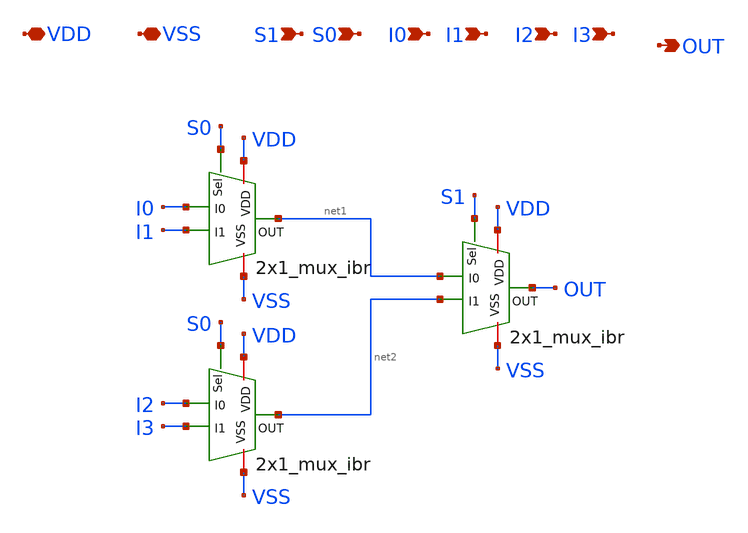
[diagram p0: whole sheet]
** sch_path: Clock_Generator_PAKISTAN_02/Schematics/4x1_mux_ibr..sch
**.subckt 4x1_mux_ibr. VDD VSS S1 OUT I2 I3 S0 I0 I1
*.iopin VDD
*.iopin VSS
*.ipin S1
*.opin OUT
*.ipin I2
*.ipin I3
*.ipin S0
*.ipin I0
*.ipin I1
x1 VSS S0 net1 I0 I1 VDD 2x1_mux_ibr
x2 VSS S0 net2 I2 I3 VDD 2x1_mux_ibr
x3 VSS S1 OUT net1 net2 VDD 2x1_mux_ibr
**.ends
.end
